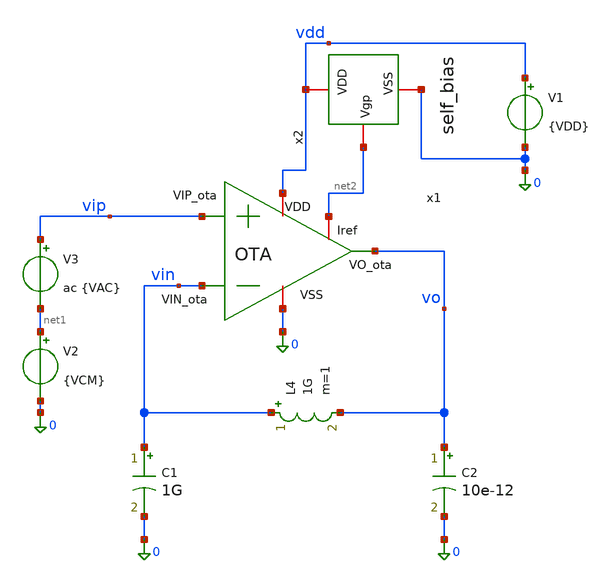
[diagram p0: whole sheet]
** sch_path: xschem/OTA_tb.sch
**.subckt OTA_tb
x1 vdd vo vin vip 0 net2 OTA
V1 vdd 0 {VDD}
V2 net1 0 {VCM}
V3 vip net1 ac {VAC}
C1 vin 0 1G m=1
L4 vin vo 1G m=1
C2 vo 0 10e-12 m=1
x2 vdd net2 0 self_bias
**** begin user architecture code




* 1. Inclusión de libreria de modelos Sky130 PRIMERO
.lib /foss/pdks/sky130A/libs.tech/ngspice/sky130.lib.spice ss
.option temp=120

**parametros_ota
.param VDD = 1.8
.param VCM = 0.6
.param VAC = 1



.control

save all
* PMOS
* --- Circuito de Polarización (Referencia) ---


* --- Etapa Diferencial (Núcleo del OTA) ---

* Mrc1 (pfet_01v8_lvt)
save @m.x1.xMrc1.msky130_fd_pr__pfet_01v8_lvt[gm]
save @m.x1.xMrc1.msky130_fd_pr__pfet_01v8_lvt[gds]
save @m.x1.xMrc1.msky130_fd_pr__pfet_01v8_lvt[id]
save @m.x1.xMrc1.msky130_fd_pr__pfet_01v8_lvt[vgs]
save @m.x1.xMrc1.msky130_fd_pr__pfet_01v8_lvt[vds]
save @m.x1.xMrc1.msky130_fd_pr__pfet_01v8_lvt[vth]
save @m.x1.xMrc1.msky130_fd_pr__pfet_01v8_lvt[vdsat]

* Mn (pfet_01v8)
save @m.x1.xMn.msky130_fd_pr__pfet_01v8_lvt[gm]
save @m.x1.xMn.msky130_fd_pr__pfet_01v8_lvt[gds]
save @m.x1.xMn.msky130_fd_pr__pfet_01v8_lvt[id]
save @m.x1.xMn.msky130_fd_pr__pfet_01v8_lvt[vgs]
save @m.x1.xMn.msky130_fd_pr__pfet_01v8_lvt[vds]
save @m.x1.xMn.msky130_fd_pr__pfet_01v8_lvt[vth]
save @m.x1.xMn.msky130_fd_pr__pfet_01v8_lvt[vdsat]

* Mp (pfet_01v8)
save @m.x1.xMp.msky130_fd_pr__pfet_01v8_lvt[gm]
save @m.x1.xMp.msky130_fd_pr__pfet_01v8_lvt[gds]
save @m.x1.xMp.msky130_fd_pr__pfet_01v8_lvt[id]
save @m.x1.xMp.msky130_fd_pr__pfet_01v8_lvt[vgs]
save @m.x1.xMp.msky130_fd_pr__pfet_01v8_lvt[vds]
save @m.x1.xMp.msky130_fd_pr__pfet_01v8_lvt[vth]
save @m.x1.xMp.msky130_fd_pr__pfet_01v8_lvt[vdsat]

* Mnr (nfet_01v8)
save @m.x1.xMnr.msky130_fd_pr__nfet_01v8[gm]
save @m.x1.xMnr.msky130_fd_pr__nfet_01v8[gds]
save @m.x1.xMnr.msky130_fd_pr__nfet_01v8[id]
save @m.x1.xMnr.msky130_fd_pr__nfet_01v8[vgs]
save @m.x1.xMnr.msky130_fd_pr__nfet_01v8[vds]
save @m.x1.xMnr.msky130_fd_pr__nfet_01v8[vth]
save @m.x1.xMnr.msky130_fd_pr__nfet_01v8[vdsat]

* Mpr (nfet_01v8)
save @m.x1.xMpr.msky130_fd_pr__nfet_01v8[gm]
save @m.x1.xMpr.msky130_fd_pr__nfet_01v8[gds]
save @m.x1.xMpr.msky130_fd_pr__nfet_01v8[id]
save @m.x1.xMpr.msky130_fd_pr__nfet_01v8[vgs]
save @m.x1.xMpr.msky130_fd_pr__nfet_01v8[vds]
save @m.x1.xMpr.msky130_fd_pr__nfet_01v8[vth]
save @m.x1.xMpr.msky130_fd_pr__nfet_01v8[vdsat]


* --- Etapa de Salida ---

* Mrc2 (pfet_01v8_lvt)
save @m.x1.xMrc2.msky130_fd_pr__pfet_01v8_lvt[gm]
save @m.x1.xMrc2.msky130_fd_pr__pfet_01v8_lvt[gds]
save @m.x1.xMrc2.msky130_fd_pr__pfet_01v8_lvt[id]
save @m.x1.xMrc2.msky130_fd_pr__pfet_01v8_lvt[vgs]
save @m.x1.xMrc2.msky130_fd_pr__pfet_01v8_lvt[vds]
save @m.x1.xMrc2.msky130_fd_pr__pfet_01v8_lvt[vth]
save @m.x1.xMrc2.msky130_fd_pr__pfet_01v8_lvt[vdsat]

* Mo (nfet_01v8)
save @m.x1.xMo.msky130_fd_pr__nfet_01v8[gm]
save @m.x1.xMo.msky130_fd_pr__nfet_01v8[gds]
save @m.x1.xMo.msky130_fd_pr__nfet_01v8[id]
save @m.x1.xMo.msky130_fd_pr__nfet_01v8[vgs]
save @m.x1.xMo.msky130_fd_pr__nfet_01v8[vds]
save @m.x1.xMo.msky130_fd_pr__nfet_01v8[vth]
save @m.x1.xMo.msky130_fd_pr__nfet_01v8[vdsat]

set filetype=ascii
op
write OTA_op.raw


ac dec 10 1 1G
write OTA_ac.raw


* 1. Frecuencia de Corte a -3dB
meas ac f3db WHEN vdb(vo) = vdb(vo)[0] - 3

* 2. UGB (Frecuencia donde la magnitud cruza 0 dB)
meas ac ugb WHEN vdb(vo) = 0

* 3. Crear el vector de fase y convertirlo a grados (multiplicando por 180/pi)
let fase_deg = cph(v(vo)) * 180 / pi

* 4. Medir la fase en grados en el punto exacto del UGB
meas ac fase_ugb FIND fase_deg WHEN vdb(vo) = 0

* 5. Calcular el Margen de Fase automáticamente
let margen_fase = 180 + fase_ugb

meas ac ganancia_banda_plana   find vdb(vo) at=10

print margen_fase
print ac ganancia_banda_plana

* 6. Graficar la magnitud y la fase ya convertida a grados
plot vdb(vo)
plot fase_deg
.endc


**** end user architecture code
**.ends

* expanding   symbol:  /foss/designs/LDO-sky130/xschem/OTA.sym # of pins=6
** sym_path: xschem/OTA.sym
** sch_path: xschem/OTA.sch
.subckt OTA VDD VO_ota VIN_ota VIP_ota VSS Iref
*.ipin VIN_ota
*.opin VO_ota
*.iopin Iref
*.iopin VSS
*.iopin VDD
*.ipin VIP_ota
XMr Iref Iref VSS VSS sky130_fd_pr__nfet_01v8 L=0.5 W=0.5 nf=1 ad='int((1 + 1)/2) * 0.5 / 1 * 0.29' as='int((1 + 2)/2) * 0.5 / 1 * 0.29'
+ pd='2*int((1 + 1)/2) * (0.5 / 1 + 0.29)' ps='2*int((1 + 2)/2) * (0.5 / 1 + 0.29)' nrd='0.29 / 0.5 ' nrs='0.29 / 0.5 '
+ sa=0 sb=0 sd=0 mult=1 m=1
XMo VO_ota VO_ota1 VDD VDD sky130_fd_pr__pfet_01v8 L=0.5 W=20 nf=1 ad='int((1 + 1)/2) * 20 / 1 * 0.29'
+ as='int((1 + 2)/2) * 20 / 1 * 0.29' pd='2*int((1 + 1)/2) * (20 / 1 + 0.29)' ps='2*int((1 + 2)/2) * (20 / 1 + 0.29)'
+ nrd='0.29 / 20 ' nrs='0.29 / 20 ' sa=0 sb=0 sd=0 mult=1 m=1
XMrc1 Vtail Iref VSS VSS sky130_fd_pr__nfet_01v8 L=0.5 W=2 nf=1 ad='int((1 + 1)/2) * 2 / 1 * 0.29' as='int((1 + 2)/2) * 2 / 1 * 0.29'
+ pd='2*int((1 + 1)/2) * (2 / 1 + 0.29)' ps='2*int((1 + 2)/2) * (2 / 1 + 0.29)' nrd='0.29 / 2 ' nrs='0.29 / 2 '
+ sa=0 sb=0 sd=0 mult=1 m=1
XMc2 VO_ota Iref VSS VSS sky130_fd_pr__nfet_01v8 L=0.5 W=1 nf=1 ad='int((1 + 1)/2) * 1 / 1 * 0.29' as='int((1 + 2)/2) * 1 / 1 * 0.29'
+ pd='2*int((1 + 1)/2) * (1 / 1 + 0.29)' ps='2*int((1 + 2)/2) * (1 / 1 + 0.29)' nrd='0.29 / 1 ' nrs='0.29 / 1 '
+ sa=0 sb=0 sd=0 mult=1 m=1
XMn VGP VIN_ota Vtail VSS sky130_fd_pr__nfet_01v8 L=0.5 W=40 nf=1 ad='int((1 + 1)/2) * 40 / 1 * 0.29'
+ as='int((1 + 2)/2) * 40 / 1 * 0.29' pd='2*int((1 + 1)/2) * (40 / 1 + 0.29)' ps='2*int((1 + 2)/2) * (40 / 1 + 0.29)'
+ nrd='0.29 / 40 ' nrs='0.29 / 40 ' sa=0 sb=0 sd=0 mult=1 m=1
XMp VO_ota1 VIP_ota Vtail VSS sky130_fd_pr__nfet_01v8 L=0.5 W=40 nf=1 ad='int((1 + 1)/2) * 40 / 1 * 0.29'
+ as='int((1 + 2)/2) * 40 / 1 * 0.29' pd='2*int((1 + 1)/2) * (40 / 1 + 0.29)' ps='2*int((1 + 2)/2) * (40 / 1 + 0.29)'
+ nrd='0.29 / 40 ' nrs='0.29 / 40 ' sa=0 sb=0 sd=0 mult=1 m=1
XMpr VO_ota1 VGP VDD VDD sky130_fd_pr__pfet_01v8 L=0.5 W=40 nf=1 ad='int((1 + 1)/2) * 40 / 1 * 0.29'
+ as='int((1 + 2)/2) * 40 / 1 * 0.29' pd='2*int((1 + 1)/2) * (40 / 1 + 0.29)' ps='2*int((1 + 2)/2) * (40 / 1 + 0.29)'
+ nrd='0.29 / 40 ' nrs='0.29 / 40 ' sa=0 sb=0 sd=0 mult=1 m=1
XMnr VGP VGP VDD VDD sky130_fd_pr__pfet_01v8 L=0.5 W=40 nf=1 ad='int((1 + 1)/2) * 40 / 1 * 0.29' as='int((1 + 2)/2) * 40 / 1 * 0.29'
+ pd='2*int((1 + 1)/2) * (40 / 1 + 0.29)' ps='2*int((1 + 2)/2) * (40 / 1 + 0.29)' nrd='0.29 / 40 ' nrs='0.29 / 40 '
+ sa=0 sb=0 sd=0 mult=1 m=1
XR1 VO_ota1 net1 VDD sky130_fd_pr__res_high_po W=0.35 L=360 mult=1 m=1
XC1 VO_ota net1 sky130_fd_pr__cap_mim_m3_2 W=50 L=50 MF=1 m=1
.ends


* expanding   symbol:  /foss/designs/OSCAR/xschem/Iref/self_bias.sym # of pins=3
** sym_path: xschem/Iref/self_bias.sym
** sch_path: xschem/Iref/self_bias.sch
.subckt self_bias VDD Vgp VSS
*.iopin Vgp
*.iopin VDD
*.iopin VSS
XMn1 VDI VR VSS VSS sky130_fd_pr__nfet_01v8 L=1 W=5 nf=1 ad='int((1 + 1)/2) * 5 / 1 * 0.29' as='int((1 + 2)/2) * 5 / 1 * 0.29'
+ pd='2*int((1 + 1)/2) * (5 / 1 + 0.29)' ps='2*int((1 + 2)/2) * (5 / 1 + 0.29)' nrd='0.29 / 5 ' nrs='0.29 / 5 '
+ sa=0 sb=0 sd=0 mult=1 m=1
XMn2 Vgp VDI VR VSS sky130_fd_pr__nfet_01v8 L=1 W=20 nf=1 ad='int((1 + 1)/2) * 20 / 1 * 0.29' as='int((1 + 2)/2) * 20 / 1 * 0.29'
+ pd='2*int((1 + 1)/2) * (20 / 1 + 0.29)' ps='2*int((1 + 2)/2) * (20 / 1 + 0.29)' nrd='0.29 / 20 ' nrs='0.29 / 20 '
+ sa=0 sb=0 sd=0 mult=1 m=1
XMs3 VDinv VR VSS VSS sky130_fd_pr__nfet_01v8 L=1 W=20 nf=1 ad='int((1 + 1)/2) * 20 / 1 * 0.29' as='int((1 + 2)/2) * 20 / 1 * 0.29'
+ pd='2*int((1 + 1)/2) * (20 / 1 + 0.29)' ps='2*int((1 + 2)/2) * (20 / 1 + 0.29)' nrd='0.29 / 20 ' nrs='0.29 / 20 '
+ sa=0 sb=0 sd=0 mult=1 m=1
XMs1 Vgp VDinv VSS VSS sky130_fd_pr__nfet_01v8 L=1 W=2 nf=1 ad='int((1 + 1)/2) * 2 / 1 * 0.29' as='int((1 + 2)/2) * 2 / 1 * 0.29'
+ pd='2*int((1 + 1)/2) * (2 / 1 + 0.29)' ps='2*int((1 + 2)/2) * (2 / 1 + 0.29)' nrd='0.29 / 2 ' nrs='0.29 / 2 '
+ sa=0 sb=0 sd=0 mult=1 m=1
XMp4 Vgp Vgp VDD VDD sky130_fd_pr__pfet_01v8_lvt L=1 W=10 nf=1 ad='int((1 + 1)/2) * 10 / 1 * 0.29' as='int((1 + 2)/2) * 10 / 1 * 0.29'
+ pd='2*int((1 + 1)/2) * (10 / 1 + 0.29)' ps='2*int((1 + 2)/2) * (10 / 1 + 0.29)' nrd='0.29 / 10 ' nrs='0.29 / 10 '
+ sa=0 sb=0 sd=0 mult=1 m=1
XMp3 VDI Vgp VDD VDD sky130_fd_pr__pfet_01v8_lvt L=1 W=10 nf=1 ad='int((1 + 1)/2) * 10 / 1 * 0.29' as='int((1 + 2)/2) * 10 / 1 * 0.29'
+ pd='2*int((1 + 1)/2) * (10 / 1 + 0.29)' ps='2*int((1 + 2)/2) * (10 / 1 + 0.29)' nrd='0.29 / 10 ' nrs='0.29 / 10 '
+ sa=0 sb=0 sd=0 mult=1 m=1
XMs2 VDinv VR VDD VDD sky130_fd_pr__pfet_01v8_lvt L=10 W=1 nf=1 ad='int((1 + 1)/2) * 1 / 1 * 0.29' as='int((1 + 2)/2) * 1 / 1 * 0.29'
+ pd='2*int((1 + 1)/2) * (1 / 1 + 0.29)' ps='2*int((1 + 2)/2) * (1 / 1 + 0.29)' nrd='0.29 / 1 ' nrs='0.29 / 1 '
+ sa=0 sb=0 sd=0 mult=1 m=1
XR1 VSS VR VSS sky130_fd_pr__res_iso_pw W=0.35 L=5.5 m=1
.ends

.end
